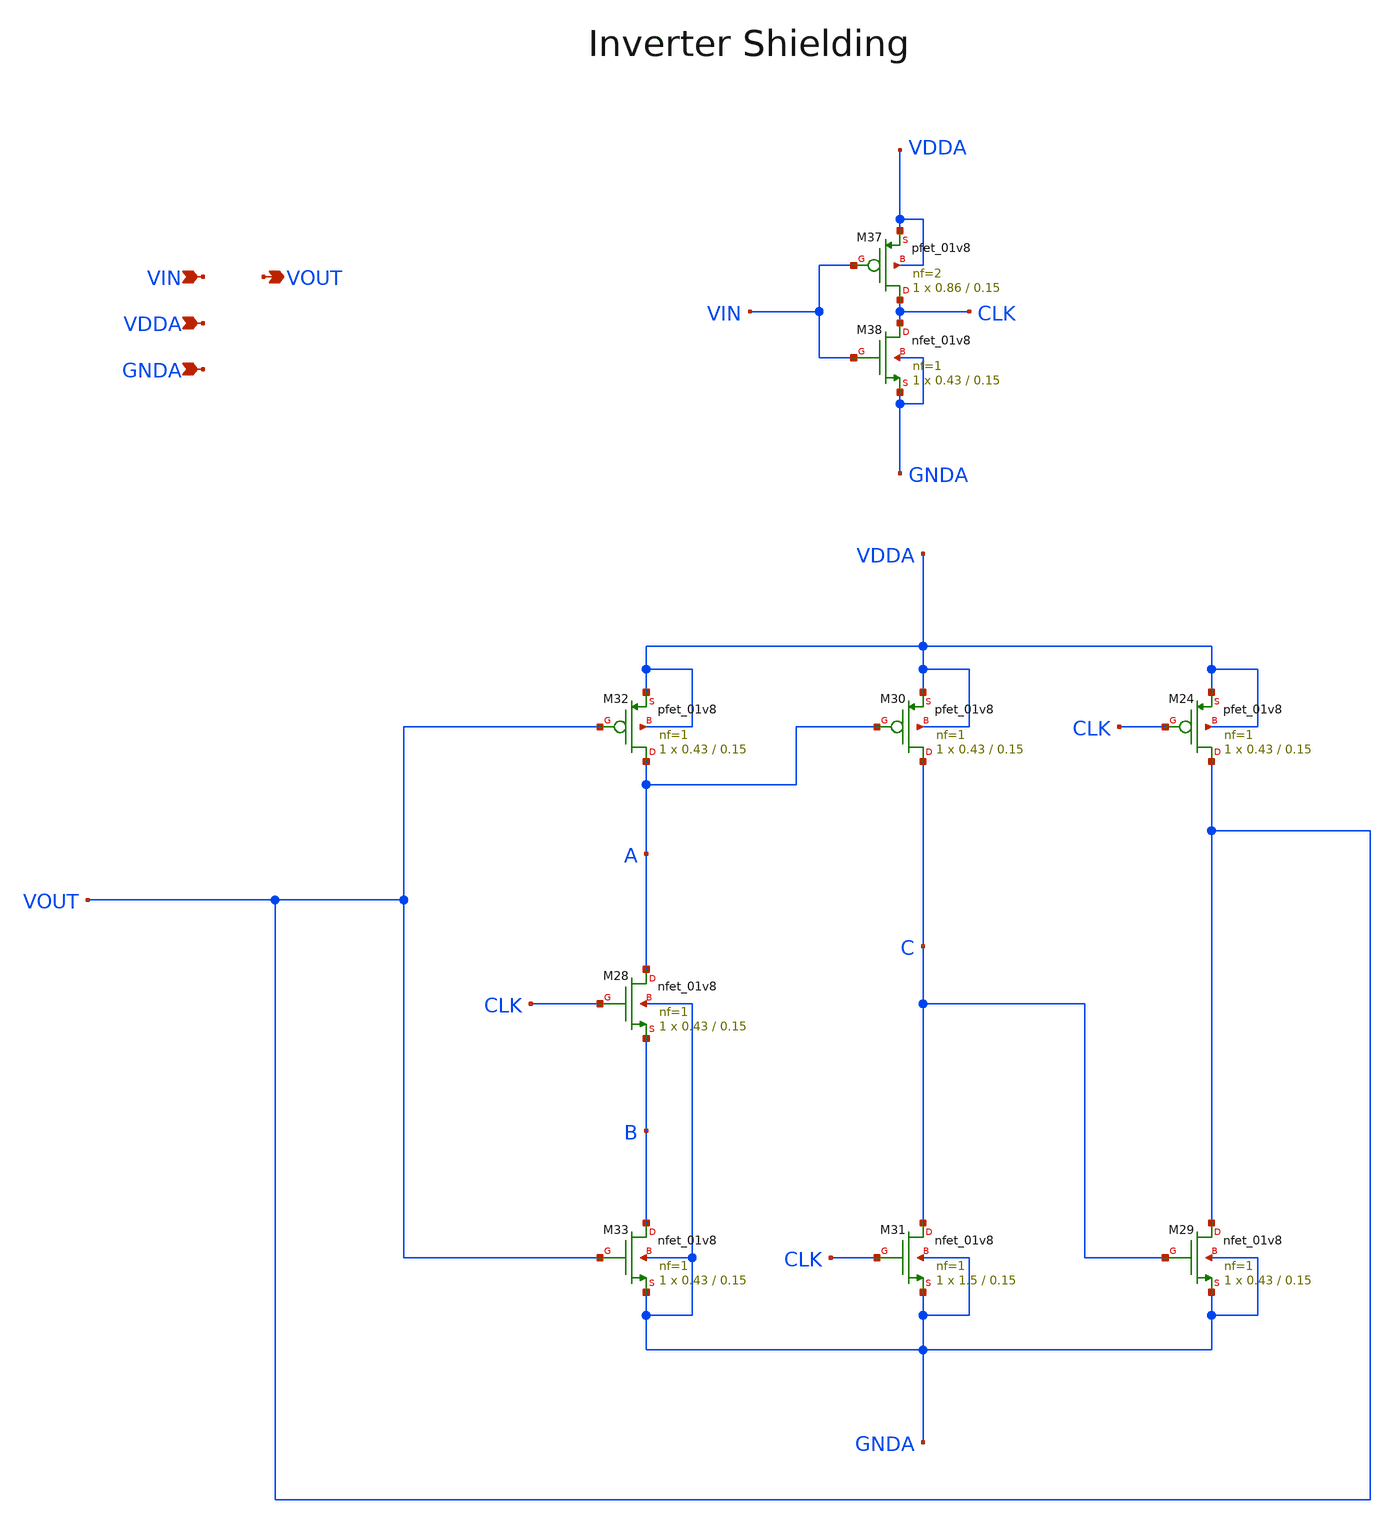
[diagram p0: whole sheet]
** sch_path: projects/pll/divider/xschem_ngspice/TSPC_FF_ratioed_divide2_2.sch
**.subckt TSPC_FF_ratioed_divide2_2 VIN VOUT VDDA GNDA
*.ipin VIN
*.opin VOUT
*.ipin VDDA
*.ipin GNDA
XM24 VOUT CLK VDDA VDDA sky130_fd_pr__pfet_01v8 L=0.15 W=0.43 nf=1 ad='int((nf+1)/2) * W/nf * 0.29' as='int((nf+2)/2) * W/nf * 0.29'
+ pd='2*int((nf+1)/2) * (W/nf + 0.29)' ps='2*int((nf+2)/2) * (W/nf + 0.29)' nrd='0.29 / W' nrs='0.29 / W'
+ sa=0 sb=0 sd=0 mult=1 m=1
XM29 VOUT C GNDA GNDA sky130_fd_pr__nfet_01v8 L=0.15 W=0.43 nf=1 ad='int((nf+1)/2) * W/nf * 0.29' as='int((nf+2)/2) * W/nf * 0.29'
+ pd='2*int((nf+1)/2) * (W/nf + 0.29)' ps='2*int((nf+2)/2) * (W/nf + 0.29)' nrd='0.29 / W' nrs='0.29 / W'
+ sa=0 sb=0 sd=0 mult=1 m=1
XM30 C A VDDA VDDA sky130_fd_pr__pfet_01v8 L=0.15 W=0.43 nf=1 ad='int((nf+1)/2) * W/nf * 0.29' as='int((nf+2)/2) * W/nf * 0.29'
+ pd='2*int((nf+1)/2) * (W/nf + 0.29)' ps='2*int((nf+2)/2) * (W/nf + 0.29)' nrd='0.29 / W' nrs='0.29 / W'
+ sa=0 sb=0 sd=0 mult=1 m=1
XM31 C CLK GNDA GNDA sky130_fd_pr__nfet_01v8 L=0.15 W=1.5 nf=1 ad='int((nf+1)/2) * W/nf * 0.29' as='int((nf+2)/2) * W/nf * 0.29'
+ pd='2*int((nf+1)/2) * (W/nf + 0.29)' ps='2*int((nf+2)/2) * (W/nf + 0.29)' nrd='0.29 / W' nrs='0.29 / W'
+ sa=0 sb=0 sd=0 mult=1 m=1
XM32 A VOUT VDDA VDDA sky130_fd_pr__pfet_01v8 L=0.15 W=0.43 nf=1 ad='int((nf+1)/2) * W/nf * 0.29' as='int((nf+2)/2) * W/nf * 0.29'
+ pd='2*int((nf+1)/2) * (W/nf + 0.29)' ps='2*int((nf+2)/2) * (W/nf + 0.29)' nrd='0.29 / W' nrs='0.29 / W'
+ sa=0 sb=0 sd=0 mult=1 m=1
XM33 B VOUT GNDA GNDA sky130_fd_pr__nfet_01v8 L=0.15 W=0.43 nf=1 ad='int((nf+1)/2) * W/nf * 0.29' as='int((nf+2)/2) * W/nf * 0.29'
+ pd='2*int((nf+1)/2) * (W/nf + 0.29)' ps='2*int((nf+2)/2) * (W/nf + 0.29)' nrd='0.29 / W' nrs='0.29 / W'
+ sa=0 sb=0 sd=0 mult=1 m=1
XM28 A CLK B GNDA sky130_fd_pr__nfet_01v8 L=0.15 W=0.43 nf=1 ad='int((nf+1)/2) * W/nf * 0.29' as='int((nf+2)/2) * W/nf * 0.29'
+ pd='2*int((nf+1)/2) * (W/nf + 0.29)' ps='2*int((nf+2)/2) * (W/nf + 0.29)' nrd='0.29 / W' nrs='0.29 / W'
+ sa=0 sb=0 sd=0 mult=1 m=1
XM37 CLK VIN VDDA VDDA sky130_fd_pr__pfet_01v8 L=0.15 W=0.86 nf=2 ad='int((nf+1)/2) * W/nf * 0.29' as='int((nf+2)/2) * W/nf * 0.29'
+ pd='2*int((nf+1)/2) * (W/nf + 0.29)' ps='2*int((nf+2)/2) * (W/nf + 0.29)' nrd='0.29 / W' nrs='0.29 / W'
+ sa=0 sb=0 sd=0 mult=1 m=1
XM38 CLK VIN GNDA GNDA sky130_fd_pr__nfet_01v8 L=0.15 W=0.43 nf=1 ad='int((nf+1)/2) * W/nf * 0.29' as='int((nf+2)/2) * W/nf * 0.29'
+ pd='2*int((nf+1)/2) * (W/nf + 0.29)' ps='2*int((nf+2)/2) * (W/nf + 0.29)' nrd='0.29 / W' nrs='0.29 / W'
+ sa=0 sb=0 sd=0 mult=1 m=1
**.ends
.end
